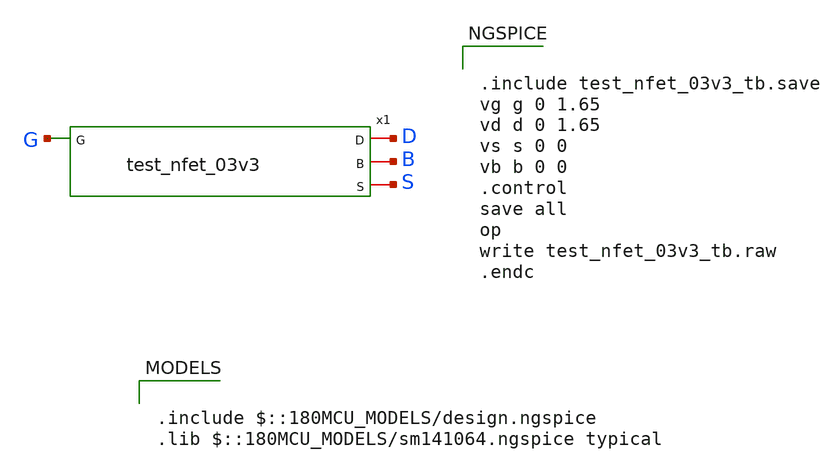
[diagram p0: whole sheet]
** sch_path: designs/libs/core_analog/saradc/tb/test_nfet_03v3_tb.sch
* designs/libs/core_analog/saradc/tb/test_nfet_03v3.sch:
* Copyright 2022 GlobalFoundries PDK Authors
* Licensed under the Apache License, Version 2.0 (the "License");
**.subckt test_nfet_03v3_tb
x1 D G B S test_nfet_03v3
**** begin user architecture code

.include $::180MCU_MODELS/design.ngspice
.lib $::180MCU_MODELS/sm141064.ngspice typical



.include test_nfet_03v3_tb.save
vg g 0 1.65
vd d 0 1.65
vs s 0 0
vb b 0 0
.control
save all
op
write test_nfet_03v3_tb.raw
.endc


**** end user architecture code
**.ends

* expanding   symbol:  test_nfet_03v3.sym # of pins=4
** sym_path: designs/libs/core_analog/saradc/tb/test_nfet_03v3.sym
** sch_path: designs/libs/core_analog/saradc/tb/test_nfet_03v3.sch
.subckt test_nfet_03v3 D G B S
*.ipin G
*.iopin D
*.iopin S
*.iopin B
XM1 D G S B nfet_03v3 L=0.28u W=0.22u nf=1 ad='int((nf+1)/2) * W/nf * 0.18u' as='int((nf+2)/2) * W/nf * 0.18u'
+ pd='2*int((nf+1)/2) * (W/nf + 0.18u)' ps='2*int((nf+2)/2) * (W/nf + 0.18u)' nrd='0.18u / W' nrs='0.18u / W'
+ sa=0 sb=0 sd=0 m=1
.ends

.end
